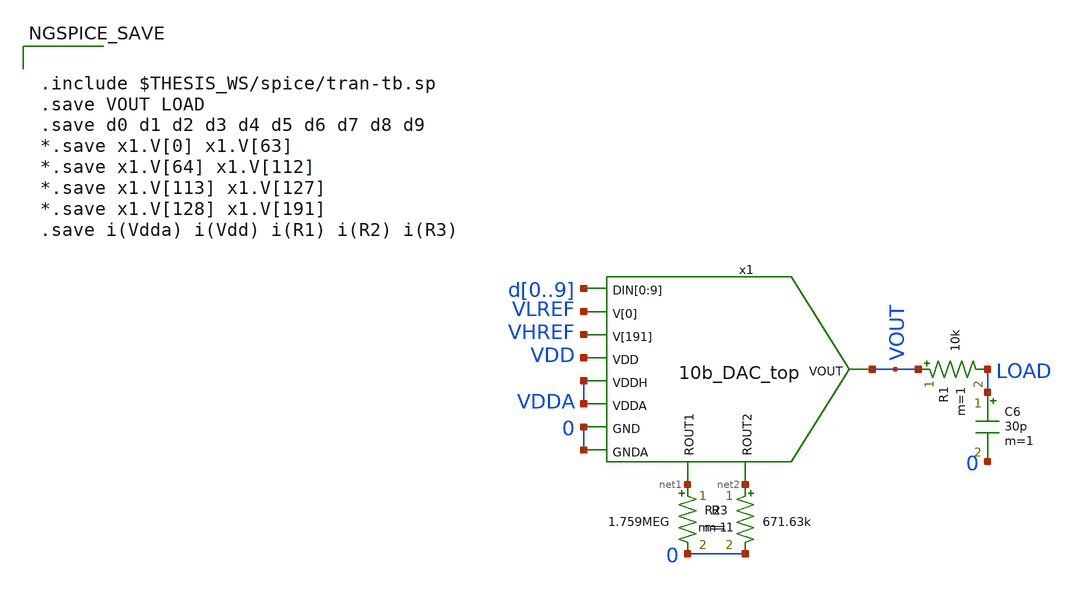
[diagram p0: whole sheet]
** sch_path: xschem/10b_DAC-tb.sch
.lib $::SKYWATER_MODELS/sky130.lib.spice tt
.include $::SKYWATER_STDCELLS/sky130_fd_sc_hd.spice
.include ~/pdk/sky130A/libs.ref/sky130_fd_sc_hvl/spice/sky130_fd_sc_hvl.spice

**.subckt 10b_DAC-tb
C6 LOAD 0 30p m=1
R1 VOUT LOAD 10k m=1
x1 d0 d1 d2 d3 d4 d5 d6 d7 d8 d9 VLREF VHREF VDD VDDA VDDA 0 0 VOUT net1 net2 10b_DAC_top
R2 net1 0 1.759MEG m=1
R3 net2 0 671.63k m=1
**** begin user architecture code


.include $THESIS_WS/spice/tran-tb.sp
.save VOUT LOAD
.save d0 d1 d2 d3 d4 d5 d6 d7 d8 d9
*.save x1.V[0] x1.V[63]
*.save x1.V[64] x1.V[112]
*.save x1.V[113] x1.V[127]
*.save x1.V[128] x1.V[191]
.save i(Vdda) i(Vdd) i(R1) i(R2) i(R3)


**** end user architecture code
**.ends
.end
